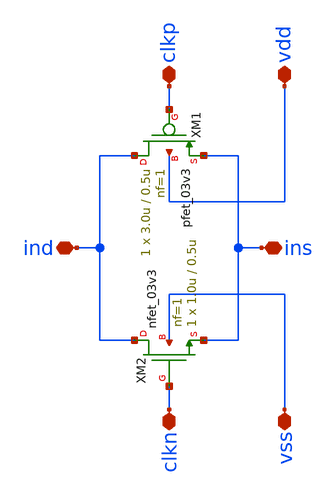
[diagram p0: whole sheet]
** sch_path: designs/libs/core_analog/transmission_gate/transmission_gate.sch
**.subckt transmission_gate ind ins clkn clkp vdd vss
*.iopin ind
*.iopin ins
*.iopin clkn
*.iopin clkp
*.iopin vdd
*.iopin vss
XM1 ind clkp ins vdd pfet_03v3 L=0.5u W=3.0u nf=1 ad='int((nf+1)/2) * W/nf * 0.18u' as='int((nf+2)/2) * W/nf * 0.18u'
+ pd='2*int((nf+1)/2) * (W/nf + 0.18u)' ps='2*int((nf+2)/2) * (W/nf + 0.18u)' nrd='0.18u / W' nrs='0.18u / W'
+ sa=0 sb=0 sd=0 m=1
XM2 ind clkn ins vss nfet_03v3 L=0.5u W=1.0u nf=1 ad='int((nf+1)/2) * W/nf * 0.18u' as='int((nf+2)/2) * W/nf * 0.18u'
+ pd='2*int((nf+1)/2) * (W/nf + 0.18u)' ps='2*int((nf+2)/2) * (W/nf + 0.18u)' nrd='0.18u / W' nrs='0.18u / W'
+ sa=0 sb=0 sd=0 m=1
**.ends
.end
